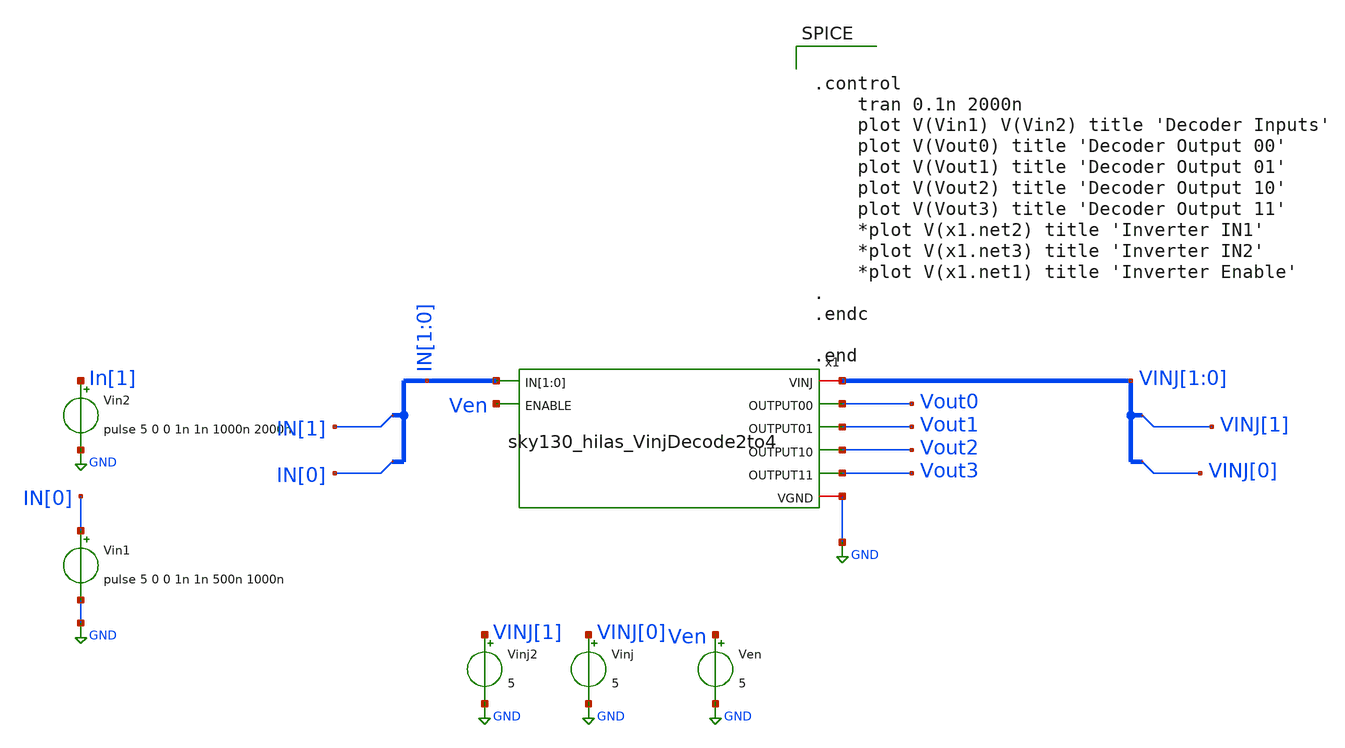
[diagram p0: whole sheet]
** sch_path: sky130_cells/RDAC/Sims/Vinj_Decode2to4_testbench.sch
**.subckt Vinj_Decode2to4_testbench
Vin1 IN[0] GND pulse 5 0 0 1n 1n 500n 1000n
Vin2 In[1] GND pulse 5 0 0 1n 1n 1000n 2000n
Vinj VINJ[0] GND 5
Ven Ven GND 5
x1 VINJ[1] IN[1] IN[0] Ven Vout0 Vout1 Vout2 Vout3 GND sky130_hilas_VinjDecode2to4
Vinj2 VINJ[1] GND 5
**** begin user architecture code


.control
	tran 0.1n 2000n
	plot V(Vin1) V(Vin2) title 'Decoder Inputs'
	plot V(Vout0) title 'Decoder Output 00'
	plot V(Vout1) title 'Decoder Output 01'
	plot V(Vout2) title 'Decoder Output 10'
	plot V(Vout3) title 'Decoder Output 11'
	*plot V(x1.net2) title 'Inverter IN1'
	*plot V(x1.net3) title 'Inverter IN2'
	*plot V(x1.net1) title 'Inverter Enable'
.
.endc

.end


** opencircuitdesign pdks install
.lib $::SKYWATER_MODELS/sky130.lib.spice tt


**** end user architecture code
**.ends

* expanding   symbol:  sky130_cells/RDAC/Design/sky130_hilas_VinjDecode2to4.sym # of pins=8
** sym_path: sky130_cells/RDAC/Design/sky130_hilas_VinjDecode2to4.sym
** sch_path: sky130_cells/RDAC/Design/sky130_hilas_VinjDecode2to4.sch
.subckt sky130_hilas_VinjDecode2to4 VINJ IN[1] IN[0] ENABLE OUTPUT00 OUTPUT01 OUTPUT10 OUTPUT11 VGND
*.ipin ENABLE
*.opin OUTPUT00
*.opin OUTPUT01
*.opin OUTPUT10
*.opin OUTPUT11
*.iopin VINJ
*.iopin VGND
*.ipin IN[1],IN[0]
x2 VINJ IN[1] VinjNOR3_2/Input2 VGND sky130_hilas_VinjInv2
x3 VINJ IN[0] VinjNOR3_1/Input1 VGND sky130_hilas_VinjInv2
x4 VINJ ENABLE VinjNOR3_3/Input3 VGND sky130_hilas_VinjInv2
x1 VINJ IN[1] IN[0] VinjNOR3_3/Input3 OUTPUT00 VGND sky130_hilas_VinjNOR3
x5 VINJ IN[1] VinjNOR3_1/Input1 VinjNOR3_3/Input3 OUTPUT01 VGND sky130_hilas_VinjNOR3
x6 VINJ VinjNOR3_2/Input2 IN[0] VinjNOR3_3/Input3 OUTPUT10 VGND sky130_hilas_VinjNOR3
x7 VINJ VinjNOR3_2/Input2 VinjNOR3_1/Input1 VinjNOR3_3/Input3 OUTPUT11 VGND sky130_hilas_VinjNOR3
.ends


* expanding   symbol:  sky130_cells/RDAC/Design/sky130_hilas_VinjInv2.sym # of pins=4
** sym_path: sky130_cells/RDAC/Design/sky130_hilas_VinjInv2.sym
** sch_path: sky130_cells/RDAC/Design/sky130_hilas_VinjInv2.sch
.subckt sky130_hilas_VinjInv2 Vinj Input Output GND
*.ipin Input
*.opin Output
*.iopin Vinj
*.iopin GND
XM4 Output Input Vinj Vinj sky130_fd_pr__pfet_g5v0d10v5 L=0.53 W=0.42 nf=1 ad='int((nf+1)/2) * W/nf * 0.29'
+ as='int((nf+2)/2) * W/nf * 0.29' pd='2*int((nf+1)/2) * (W/nf + 0.29)' ps='2*int((nf+2)/2) * (W/nf + 0.29)'
+ nrd='0.29 / W' nrs='0.29 / W' sa=0 sb=0 sd=0 mult=1 m=1
XM3 Output Input GND GND sky130_fd_pr__nfet_g5v0d10v5 L=0.52 W=0.42 nf=1 ad='int((nf+1)/2) * W/nf * 0.29'
+ as='int((nf+2)/2) * W/nf * 0.29' pd='2*int((nf+1)/2) * (W/nf + 0.29)' ps='2*int((nf+2)/2) * (W/nf + 0.29)'
+ nrd='0.29 / W' nrs='0.29 / W' sa=0 sb=0 sd=0 mult=1 m=1
.ends


* expanding   symbol:  sky130_cells/RDAC/Design/sky130_hilas_VinjNOR3.sym # of pins=6
** sym_path: sky130_cells/RDAC/Design/sky130_hilas_VinjNOR3.sym
** sch_path: sky130_cells/RDAC/Design/sky130_hilas_VinjNOR3.sch
.subckt sky130_hilas_VinjNOR3 Vinj Input1 Input2 Input3 OUTPUT GND
*.ipin Input3
*.ipin Input1
*.ipin Input2
*.iopin Vinj
*.iopin GND
*.opin OUTPUT
XM1 OUTPUT Input3 GND GND sky130_fd_pr__nfet_g5v0d10v5 L=0.5 W=0.42 nf=1 ad='int((nf+1)/2) * W/nf * 0.29'
+ as='int((nf+2)/2) * W/nf * 0.29' pd='2*int((nf+1)/2) * (W/nf + 0.29)' ps='2*int((nf+2)/2) * (W/nf + 0.29)'
+ nrd='0.29 / W' nrs='0.29 / W' sa=0 sb=0 sd=0 mult=1 m=1
XM2 OUTPUT Input1 GND GND sky130_fd_pr__nfet_g5v0d10v5 L=0.51 W=0.43 nf=1 ad='int((nf+1)/2) * W/nf * 0.29'
+ as='int((nf+2)/2) * W/nf * 0.29' pd='2*int((nf+1)/2) * (W/nf + 0.29)' ps='2*int((nf+2)/2) * (W/nf + 0.29)'
+ nrd='0.29 / W' nrs='0.29 / W' sa=0 sb=0 sd=0 mult=1 m=1
XM3 OUTPUT Input2 GND GND sky130_fd_pr__nfet_g5v0d10v5 L=0.5 W=0.42 nf=1 ad='int((nf+1)/2) * W/nf * 0.29'
+ as='int((nf+2)/2) * W/nf * 0.29' pd='2*int((nf+1)/2) * (W/nf + 0.29)' ps='2*int((nf+2)/2) * (W/nf + 0.29)'
+ nrd='0.29 / W' nrs='0.29 / W' sa=0 sb=0 sd=0 mult=1 m=1
XM6 OUTPUT Input2 net2 Vinj sky130_fd_pr__pfet_g5v0d10v5 L=0.52 W=0.43 nf=1 ad='int((nf+1)/2) * W/nf * 0.29'
+ as='int((nf+2)/2) * W/nf * 0.29' pd='2*int((nf+1)/2) * (W/nf + 0.29)' ps='2*int((nf+2)/2) * (W/nf + 0.29)'
+ nrd='0.29 / W' nrs='0.29 / W' sa=0 sb=0 sd=0 mult=1 m=1
XM4 net2 Input1 net1 Vinj sky130_fd_pr__pfet_g5v0d10v5 L=0.52 W=0.42 nf=1 ad='int((nf+1)/2) * W/nf * 0.29'
+ as='int((nf+2)/2) * W/nf * 0.29' pd='2*int((nf+1)/2) * (W/nf + 0.29)' ps='2*int((nf+2)/2) * (W/nf + 0.29)'
+ nrd='0.29 / W' nrs='0.29 / W' sa=0 sb=0 sd=0 mult=1 m=1
XM5 net1 Input3 Vinj Vinj sky130_fd_pr__pfet_g5v0d10v5 L=0.53 W=0.42 nf=1 ad='int((nf+1)/2) * W/nf * 0.29'
+ as='int((nf+2)/2) * W/nf * 0.29' pd='2*int((nf+1)/2) * (W/nf + 0.29)' ps='2*int((nf+2)/2) * (W/nf + 0.29)'
+ nrd='0.29 / W' nrs='0.29 / W' sa=0 sb=0 sd=0 mult=1 m=1
.ends

.GLOBAL GND
.end
